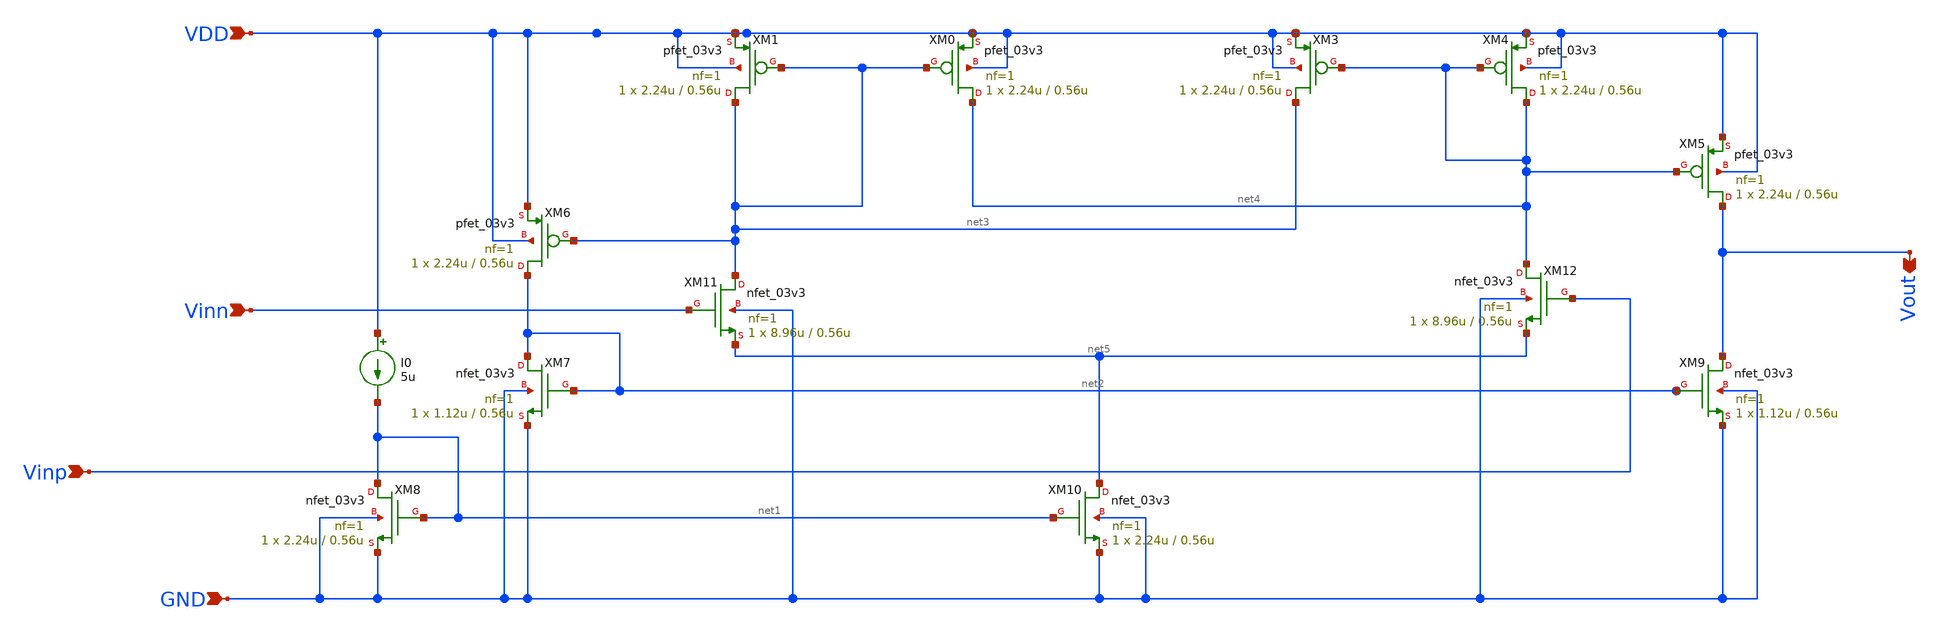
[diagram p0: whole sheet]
** sch_path: comparator/schematic-design/comp_forsym.sch
**.subckt comp_forsym Vout Vinn Vinp VDD GND
*.opin Vout
*.ipin Vinn
*.ipin Vinp
*.ipin VDD
*.ipin GND
XM1 net3 net3 VDD VDD pfet_03v3 L=0.56u W=2.24u nf=1 ad='int((nf+1)/2) * W/nf * 0.18u' as='int((nf+2)/2) * W/nf * 0.18u'
+ pd='2*int((nf+1)/2) * (W/nf + 0.18u)' ps='2*int((nf+2)/2) * (W/nf + 0.18u)' nrd='0.18u / W' nrs='0.18u / W'
+ sa=0 sb=0 sd=0 m=1
XM0 net4 net3 VDD VDD pfet_03v3 L=0.56u W=2.24u nf=1 ad='int((nf+1)/2) * W/nf * 0.18u' as='int((nf+2)/2) * W/nf * 0.18u'
+ pd='2*int((nf+1)/2) * (W/nf + 0.18u)' ps='2*int((nf+2)/2) * (W/nf + 0.18u)' nrd='0.18u / W' nrs='0.18u / W'
+ sa=0 sb=0 sd=0 m=1
XM3 net3 net4 VDD VDD pfet_03v3 L=0.56u W=2.24u nf=1 ad='int((nf+1)/2) * W/nf * 0.18u' as='int((nf+2)/2) * W/nf * 0.18u'
+ pd='2*int((nf+1)/2) * (W/nf + 0.18u)' ps='2*int((nf+2)/2) * (W/nf + 0.18u)' nrd='0.18u / W' nrs='0.18u / W'
+ sa=0 sb=0 sd=0 m=1
XM4 net4 net4 VDD VDD pfet_03v3 L=0.56u W=2.24u nf=1 ad='int((nf+1)/2) * W/nf * 0.18u' as='int((nf+2)/2) * W/nf * 0.18u'
+ pd='2*int((nf+1)/2) * (W/nf + 0.18u)' ps='2*int((nf+2)/2) * (W/nf + 0.18u)' nrd='0.18u / W' nrs='0.18u / W'
+ sa=0 sb=0 sd=0 m=1
XM5 Vout net4 VDD VDD pfet_03v3 L=0.56u W=2.24u nf=1 ad='int((nf+1)/2) * W/nf * 0.18u' as='int((nf+2)/2) * W/nf * 0.18u'
+ pd='2*int((nf+1)/2) * (W/nf + 0.18u)' ps='2*int((nf+2)/2) * (W/nf + 0.18u)' nrd='0.18u / W' nrs='0.18u / W'
+ sa=0 sb=0 sd=0 m=1
XM6 net2 net3 VDD VDD pfet_03v3 L=0.56u W=2.24u nf=1 ad='int((nf+1)/2) * W/nf * 0.18u' as='int((nf+2)/2) * W/nf * 0.18u'
+ pd='2*int((nf+1)/2) * (W/nf + 0.18u)' ps='2*int((nf+2)/2) * (W/nf + 0.18u)' nrd='0.18u / W' nrs='0.18u / W'
+ sa=0 sb=0 sd=0 m=1
XM7 net2 net2 GND GND nfet_03v3 L=0.56u W=1.12u nf=1 ad='int((nf+1)/2) * W/nf * 0.18u' as='int((nf+2)/2) * W/nf * 0.18u'
+ pd='2*int((nf+1)/2) * (W/nf + 0.18u)' ps='2*int((nf+2)/2) * (W/nf + 0.18u)' nrd='0.18u / W' nrs='0.18u / W'
+ sa=0 sb=0 sd=0 m=1
XM8 net1 net1 GND GND nfet_03v3 L=0.56u W=2.24u nf=1 ad='int((nf+1)/2) * W/nf * 0.18u' as='int((nf+2)/2) * W/nf * 0.18u'
+ pd='2*int((nf+1)/2) * (W/nf + 0.18u)' ps='2*int((nf+2)/2) * (W/nf + 0.18u)' nrd='0.18u / W' nrs='0.18u / W'
+ sa=0 sb=0 sd=0 m=1
XM9 Vout net2 GND GND nfet_03v3 L=0.56u W=1.12u nf=1 ad='int((nf+1)/2) * W/nf * 0.18u' as='int((nf+2)/2) * W/nf * 0.18u'
+ pd='2*int((nf+1)/2) * (W/nf + 0.18u)' ps='2*int((nf+2)/2) * (W/nf + 0.18u)' nrd='0.18u / W' nrs='0.18u / W'
+ sa=0 sb=0 sd=0 m=1
XM10 net5 net1 GND GND nfet_03v3 L=0.56u W=2.24u nf=1 ad='int((nf+1)/2) * W/nf * 0.18u' as='int((nf+2)/2) * W/nf * 0.18u'
+ pd='2*int((nf+1)/2) * (W/nf + 0.18u)' ps='2*int((nf+2)/2) * (W/nf + 0.18u)' nrd='0.18u / W' nrs='0.18u / W'
+ sa=0 sb=0 sd=0 m=1
XM11 net3 Vinn net5 GND nfet_03v3 L=0.56u W=8.96u nf=1 ad='int((nf+1)/2) * W/nf * 0.18u' as='int((nf+2)/2) * W/nf * 0.18u'
+ pd='2*int((nf+1)/2) * (W/nf + 0.18u)' ps='2*int((nf+2)/2) * (W/nf + 0.18u)' nrd='0.18u / W' nrs='0.18u / W'
+ sa=0 sb=0 sd=0 m=1
XM12 net4 Vinp net5 GND nfet_03v3 L=0.56u W=8.96u nf=1 ad='int((nf+1)/2) * W/nf * 0.18u' as='int((nf+2)/2) * W/nf * 0.18u'
+ pd='2*int((nf+1)/2) * (W/nf + 0.18u)' ps='2*int((nf+2)/2) * (W/nf + 0.18u)' nrd='0.18u / W' nrs='0.18u / W'
+ sa=0 sb=0 sd=0 m=1
I0 VDD net1 5u
**.ends
.end
